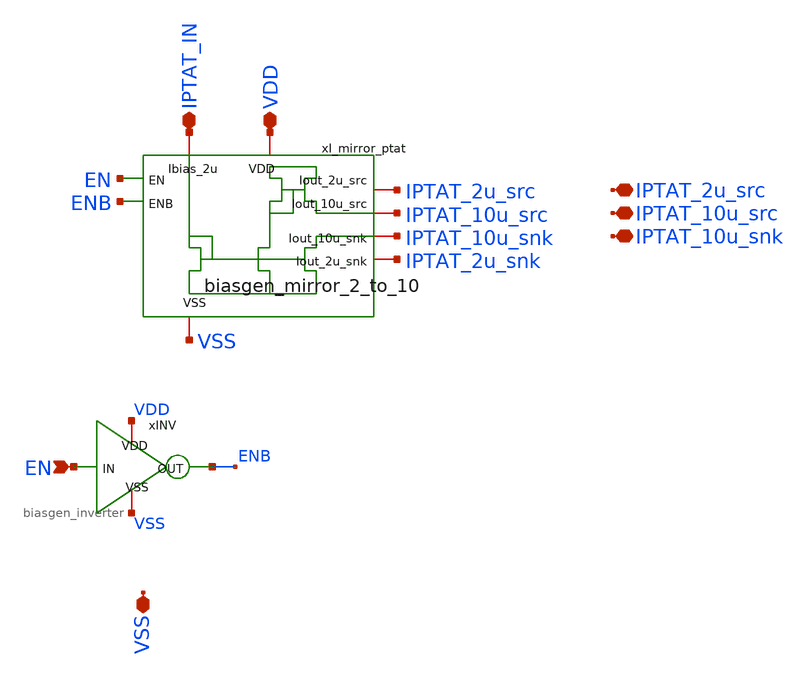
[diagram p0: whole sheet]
** sch_path: designs/libs/core_biasgen/biasgen_v2/biasgen_v2.sch
**.subckt biasgen_v2 VSS IPTAT_IN IPTAT_2u_src IPTAT_10u_snk VDD EN IPTAT_10u_src
*.iopin VSS
*.iopin IPTAT_IN
*.iopin IPTAT_2u_src
*.iopin IPTAT_10u_snk
*.iopin VDD
*.ipin EN
*.iopin IPTAT_10u_src
xI_mirror_ptat VDD IPTAT_IN EN ENB IPTAT_10u_src IPTAT_10u_snk VSS IPTAT_2u_src IPTAT_2u_snk
+ biasgen_mirror_2_to_10
xINV VDD EN ENB VSS biasgen_inverter
**.ends

* expanding   symbol:  libs/core_biasgen/biasgen_mirror_2_to_10/biasgen_mirror_2_to_10.sym # of
*+ pins=9
** sym_path: designs/libs/core_biasgen/biasgen_mirror_2_to_10/biasgen_mirror_2_to_10.sym
** sch_path: designs/libs/core_biasgen/biasgen_mirror_2_to_10/biasgen_mirror_2_to_10.sch
.subckt biasgen_mirror_2_to_10 VDD Ibias_2u EN ENB Iout_10u_src Iout_10u_snk VSS Iout_2u_src
+ Iout_2u_snk
*.iopin Ibias_2u
*.iopin VDD
*.iopin VSS
*.iopin Iout_10u_snk
*.iopin Iout_10u_src
*.ipin EN
*.ipin ENB
*.iopin Iout_2u_src
*.iopin Iout_2u_snk
XMnref0 net1 vnref VSS VSS nfet_05v0 L=2u W=0.5u nf=1 ad='int((nf+1)/2) * W/nf * 0.18u' as='int((nf+2)/2) * W/nf * 0.18u'
+ pd='2*int((nf+1)/2) * (W/nf + 0.18u)' ps='2*int((nf+2)/2) * (W/nf + 0.18u)' nrd='0.18u / W' nrs='0.18u / W'
+ sa=0 sb=0 sd=0 m=2
XMncas0 vnref vncas net1 VSS nfet_05v0 L=0.8u W=0.5u nf=1 ad='int((nf+1)/2) * W/nf * 0.18u' as='int((nf+2)/2) * W/nf * 0.18u'
+ pd='2*int((nf+1)/2) * (W/nf + 0.18u)' ps='2*int((nf+2)/2) * (W/nf + 0.18u)' nrd='0.18u / W' nrs='0.18u / W'
+ sa=0 sb=0 sd=0 m=2
XMnenbias Ibias_2u EN vncas vncas nfet_05v0 L=0.6u W=2u nf=1 ad='int((nf+1)/2) * W/nf * 0.18u' as='int((nf+2)/2) * W/nf * 0.18u'
+ pd='2*int((nf+1)/2) * (W/nf + 0.18u)' ps='2*int((nf+2)/2) * (W/nf + 0.18u)' nrd='0.18u / W' nrs='0.18u / W'
+ sa=0 sb=0 sd=0 m=1
XMnref1 net2 vnref VSS VSS nfet_05v0 L=2u W=0.5u nf=1 ad='int((nf+1)/2) * W/nf * 0.18u' as='int((nf+2)/2) * W/nf * 0.18u'
+ pd='2*int((nf+1)/2) * (W/nf + 0.18u)' ps='2*int((nf+2)/2) * (W/nf + 0.18u)' nrd='0.18u / W' nrs='0.18u / W'
+ sa=0 sb=0 sd=0 m=2
XMncas1 vpcas vncas net2 VSS nfet_05v0 L=0.8u W=0.5u nf=1 ad='int((nf+1)/2) * W/nf * 0.18u' as='int((nf+2)/2) * W/nf * 0.18u'
+ pd='2*int((nf+1)/2) * (W/nf + 0.18u)' ps='2*int((nf+2)/2) * (W/nf + 0.18u)' nrd='0.18u / W' nrs='0.18u / W'
+ sa=0 sb=0 sd=0 m=2
XMpref1 net3 vpref VDD VDD pfet_05v0 L=1.5u W=1u nf=1 ad='int((nf+1)/2) * W/nf * 0.18u' as='int((nf+2)/2) * W/nf * 0.18u'
+ pd='2*int((nf+1)/2) * (W/nf + 0.18u)' ps='2*int((nf+2)/2) * (W/nf + 0.18u)' nrd='0.18u / W' nrs='0.18u / W'
+ sa=0 sb=0 sd=0 m=2
XMpcas0 vpref vpcas net3 VDD pfet_05v0 L=0.8u W=1u nf=1 ad='int((nf+1)/2) * W/nf * 0.18u' as='int((nf+2)/2) * W/nf * 0.18u'
+ pd='2*int((nf+1)/2) * (W/nf + 0.18u)' ps='2*int((nf+2)/2) * (W/nf + 0.18u)' nrd='0.18u / W' nrs='0.18u / W'
+ sa=0 sb=0 sd=0 m=2
XMpcas1 vpcas vpcas VDD VDD pfet_05v0 L=6u W=1u nf=1 ad='int((nf+1)/2) * W/nf * 0.18u' as='int((nf+2)/2) * W/nf * 0.18u'
+ pd='2*int((nf+1)/2) * (W/nf + 0.18u)' ps='2*int((nf+2)/2) * (W/nf + 0.18u)' nrd='0.18u / W' nrs='0.18u / W'
+ sa=0 sb=0 sd=0 m=2
XMnref2 net4 vnref VSS VSS nfet_05v0 L=2u W=0.5u nf=1 ad='int((nf+1)/2) * W/nf * 0.18u' as='int((nf+2)/2) * W/nf * 0.18u'
+ pd='2*int((nf+1)/2) * (W/nf + 0.18u)' ps='2*int((nf+2)/2) * (W/nf + 0.18u)' nrd='0.18u / W' nrs='0.18u / W'
+ sa=0 sb=0 sd=0 m=2
XMncas2 vpref vncas net4 VSS nfet_05v0 L=0.8u W=0.5u nf=1 ad='int((nf+1)/2) * W/nf * 0.18u' as='int((nf+2)/2) * W/nf * 0.18u'
+ pd='2*int((nf+1)/2) * (W/nf + 0.18u)' ps='2*int((nf+2)/2) * (W/nf + 0.18u)' nrd='0.18u / W' nrs='0.18u / W'
+ sa=0 sb=0 sd=0 m=2
XMpref2 net5 vpref VDD VDD pfet_05v0 L=1.5u W=1u nf=1 ad='int((nf+1)/2) * W/nf * 0.18u' as='int((nf+2)/2) * W/nf * 0.18u'
+ pd='2*int((nf+1)/2) * (W/nf + 0.18u)' ps='2*int((nf+2)/2) * (W/nf + 0.18u)' nrd='0.18u / W' nrs='0.18u / W'
+ sa=0 sb=0 sd=0 m=10
XMpcas2 Iout_10u_src vpcas net5 VDD pfet_05v0 L=0.8u W=1u nf=1 ad='int((nf+1)/2) * W/nf * 0.18u' as='int((nf+2)/2) * W/nf * 0.18u'
+ pd='2*int((nf+1)/2) * (W/nf + 0.18u)' ps='2*int((nf+2)/2) * (W/nf + 0.18u)' nrd='0.18u / W' nrs='0.18u / W'
+ sa=0 sb=0 sd=0 m=10
XMnref3 net6 vnref VSS VSS nfet_05v0 L=2u W=0.5u nf=1 ad='int((nf+1)/2) * W/nf * 0.18u' as='int((nf+2)/2) * W/nf * 0.18u'
+ pd='2*int((nf+1)/2) * (W/nf + 0.18u)' ps='2*int((nf+2)/2) * (W/nf + 0.18u)' nrd='0.18u / W' nrs='0.18u / W'
+ sa=0 sb=0 sd=0 m=10
XMncas3 Iout_10u_snk vncas net6 VSS nfet_05v0 L=0.8u W=0.5u nf=1 ad='int((nf+1)/2) * W/nf * 0.18u' as='int((nf+2)/2) * W/nf * 0.18u'
+ pd='2*int((nf+1)/2) * (W/nf + 0.18u)' ps='2*int((nf+2)/2) * (W/nf + 0.18u)' nrd='0.18u / W' nrs='0.18u / W'
+ sa=0 sb=0 sd=0 m=10
XMnennref vnref ENB VSS VSS nfet_05v0 L=0.6u W=2u nf=1 ad='int((nf+1)/2) * W/nf * 0.18u' as='int((nf+2)/2) * W/nf * 0.18u'
+ pd='2*int((nf+1)/2) * (W/nf + 0.18u)' ps='2*int((nf+2)/2) * (W/nf + 0.18u)' nrd='0.18u / W' nrs='0.18u / W'
+ sa=0 sb=0 sd=0 m=1
XMnenncas vncas ENB VSS VSS nfet_05v0 L=0.6u W=2u nf=1 ad='int((nf+1)/2) * W/nf * 0.18u' as='int((nf+2)/2) * W/nf * 0.18u'
+ pd='2*int((nf+1)/2) * (W/nf + 0.18u)' ps='2*int((nf+2)/2) * (W/nf + 0.18u)' nrd='0.18u / W' nrs='0.18u / W'
+ sa=0 sb=0 sd=0 m=1
XMpcas3 vpref EN VDD VDD pfet_05v0 L=0.5u W=1u nf=1 ad='int((nf+1)/2) * W/nf * 0.18u' as='int((nf+2)/2) * W/nf * 0.18u'
+ pd='2*int((nf+1)/2) * (W/nf + 0.18u)' ps='2*int((nf+2)/2) * (W/nf + 0.18u)' nrd='0.18u / W' nrs='0.18u / W'
+ sa=0 sb=0 sd=0 m=1
XMpcas4 vpcas EN VDD VDD pfet_05v0 L=0.5u W=1u nf=1 ad='int((nf+1)/2) * W/nf * 0.18u' as='int((nf+2)/2) * W/nf * 0.18u'
+ pd='2*int((nf+1)/2) * (W/nf + 0.18u)' ps='2*int((nf+2)/2) * (W/nf + 0.18u)' nrd='0.18u / W' nrs='0.18u / W'
+ sa=0 sb=0 sd=0 m=1
XMpref3 net7 vpref VDD VDD pfet_05v0 L=1.5u W=1u nf=1 ad='int((nf+1)/2) * W/nf * 0.18u' as='int((nf+2)/2) * W/nf * 0.18u'
+ pd='2*int((nf+1)/2) * (W/nf + 0.18u)' ps='2*int((nf+2)/2) * (W/nf + 0.18u)' nrd='0.18u / W' nrs='0.18u / W'
+ sa=0 sb=0 sd=0 m=2
XMpcas5 Iout_2u_src vpcas net7 VDD pfet_05v0 L=0.8u W=1u nf=1 ad='int((nf+1)/2) * W/nf * 0.18u' as='int((nf+2)/2) * W/nf * 0.18u'
+ pd='2*int((nf+1)/2) * (W/nf + 0.18u)' ps='2*int((nf+2)/2) * (W/nf + 0.18u)' nrd='0.18u / W' nrs='0.18u / W'
+ sa=0 sb=0 sd=0 m=2
XMnref4 net8 vnref VSS VSS nfet_05v0 L=2u W=0.5u nf=1 ad='int((nf+1)/2) * W/nf * 0.18u' as='int((nf+2)/2) * W/nf * 0.18u'
+ pd='2*int((nf+1)/2) * (W/nf + 0.18u)' ps='2*int((nf+2)/2) * (W/nf + 0.18u)' nrd='0.18u / W' nrs='0.18u / W'
+ sa=0 sb=0 sd=0 m=2
XMncas4 Iout_2u_snk vncas net8 VSS nfet_05v0 L=0.8u W=0.5u nf=1 ad='int((nf+1)/2) * W/nf * 0.18u' as='int((nf+2)/2) * W/nf * 0.18u'
+ pd='2*int((nf+1)/2) * (W/nf + 0.18u)' ps='2*int((nf+2)/2) * (W/nf + 0.18u)' nrd='0.18u / W' nrs='0.18u / W'
+ sa=0 sb=0 sd=0 m=2
XMnref_dumm_L VSS VSS VSS VSS nfet_05v0 L=2u W=0.5u nf=1 ad='int((nf+1)/2) * W/nf * 0.18u' as='int((nf+2)/2) * W/nf * 0.18u'
+ pd='2*int((nf+1)/2) * (W/nf + 0.18u)' ps='2*int((nf+2)/2) * (W/nf + 0.18u)' nrd='0.18u / W' nrs='0.18u / W'
+ sa=0 sb=0 sd=0 m=2
XMncas_dumm_L VSS VSS VSS VSS nfet_05v0 L=0.8u W=0.5u nf=1 ad='int((nf+1)/2) * W/nf * 0.18u' as='int((nf+2)/2) * W/nf * 0.18u'
+ pd='2*int((nf+1)/2) * (W/nf + 0.18u)' ps='2*int((nf+2)/2) * (W/nf + 0.18u)' nrd='0.18u / W' nrs='0.18u / W'
+ sa=0 sb=0 sd=0 m=2
XMpref_dumm_L[1] VDD VDD VDD VDD pfet_05v0 L=1.5u W=1u nf=1 ad='int((nf+1)/2) * W/nf * 0.18u' as='int((nf+2)/2) * W/nf * 0.18u'
+ pd='2*int((nf+1)/2) * (W/nf + 0.18u)' ps='2*int((nf+2)/2) * (W/nf + 0.18u)' nrd='0.18u / W' nrs='0.18u / W'
+ sa=0 sb=0 sd=0 m=1
XMpref_dumm_L[0] VDD VDD VDD VDD pfet_05v0 L=1.5u W=1u nf=1 ad='int((nf+1)/2) * W/nf * 0.18u' as='int((nf+2)/2) * W/nf * 0.18u'
+ pd='2*int((nf+1)/2) * (W/nf + 0.18u)' ps='2*int((nf+2)/2) * (W/nf + 0.18u)' nrd='0.18u / W' nrs='0.18u / W'
+ sa=0 sb=0 sd=0 m=1
XMpcas_dumm_L[1] VDD VDD VDD VDD pfet_05v0 L=0.8u W=1u nf=1 ad='int((nf+1)/2) * W/nf * 0.18u' as='int((nf+2)/2) * W/nf * 0.18u'
+ pd='2*int((nf+1)/2) * (W/nf + 0.18u)' ps='2*int((nf+2)/2) * (W/nf + 0.18u)' nrd='0.18u / W' nrs='0.18u / W'
+ sa=0 sb=0 sd=0 m=1
XMpcas_dumm_L[0] VDD VDD VDD VDD pfet_05v0 L=0.8u W=1u nf=1 ad='int((nf+1)/2) * W/nf * 0.18u' as='int((nf+2)/2) * W/nf * 0.18u'
+ pd='2*int((nf+1)/2) * (W/nf + 0.18u)' ps='2*int((nf+2)/2) * (W/nf + 0.18u)' nrd='0.18u / W' nrs='0.18u / W'
+ sa=0 sb=0 sd=0 m=1
XMpcasref_dumm_L[3] VDD VDD VDD VDD pfet_05v0 L=6u W=1u nf=1 ad='int((nf+1)/2) * W/nf * 0.18u' as='int((nf+2)/2) * W/nf * 0.18u'
+ pd='2*int((nf+1)/2) * (W/nf + 0.18u)' ps='2*int((nf+2)/2) * (W/nf + 0.18u)' nrd='0.18u / W' nrs='0.18u / W'
+ sa=0 sb=0 sd=0 m=1
XMpcasref_dumm_L[2] VDD VDD VDD VDD pfet_05v0 L=6u W=1u nf=1 ad='int((nf+1)/2) * W/nf * 0.18u' as='int((nf+2)/2) * W/nf * 0.18u'
+ pd='2*int((nf+1)/2) * (W/nf + 0.18u)' ps='2*int((nf+2)/2) * (W/nf + 0.18u)' nrd='0.18u / W' nrs='0.18u / W'
+ sa=0 sb=0 sd=0 m=1
XMpcasref_dumm_L[1] VDD VDD VDD VDD pfet_05v0 L=6u W=1u nf=1 ad='int((nf+1)/2) * W/nf * 0.18u' as='int((nf+2)/2) * W/nf * 0.18u'
+ pd='2*int((nf+1)/2) * (W/nf + 0.18u)' ps='2*int((nf+2)/2) * (W/nf + 0.18u)' nrd='0.18u / W' nrs='0.18u / W'
+ sa=0 sb=0 sd=0 m=1
XMpcasref_dumm_L[0] VDD VDD VDD VDD pfet_05v0 L=6u W=1u nf=1 ad='int((nf+1)/2) * W/nf * 0.18u' as='int((nf+2)/2) * W/nf * 0.18u'
+ pd='2*int((nf+1)/2) * (W/nf + 0.18u)' ps='2*int((nf+2)/2) * (W/nf + 0.18u)' nrd='0.18u / W' nrs='0.18u / W'
+ sa=0 sb=0 sd=0 m=1
XRPcas[7] vr_ncas[7] vncas VSS ppolyf_u_1k_6p0 r_width=1e-6 r_length=4.5e-6 m=1
XRPcas[6] vr_ncas[6] vr_ncas[7] VSS ppolyf_u_1k_6p0 r_width=1e-6 r_length=4.5e-6 m=1
XRPcas[5] vr_ncas[5] vr_ncas[6] VSS ppolyf_u_1k_6p0 r_width=1e-6 r_length=4.5e-6 m=1
XRPcas[4] vr_ncas[4] vr_ncas[5] VSS ppolyf_u_1k_6p0 r_width=1e-6 r_length=4.5e-6 m=1
XRPcas[3] vr_ncas[3] vr_ncas[4] VSS ppolyf_u_1k_6p0 r_width=1e-6 r_length=4.5e-6 m=1
XRPcas[2] vr_ncas[2] vr_ncas[3] VSS ppolyf_u_1k_6p0 r_width=1e-6 r_length=4.5e-6 m=1
XRPcas[1] vr_ncas[1] vr_ncas[2] VSS ppolyf_u_1k_6p0 r_width=1e-6 r_length=4.5e-6 m=1
XRPcas[0] vnref vr_ncas[1] VSS ppolyf_u_1k_6p0 r_width=1e-6 r_length=4.5e-6 m=1
.ends


* expanding   symbol:  libs/core_biasgen/biasgen_inverter/biasgen_inverter.sym # of pins=4
** sym_path: designs/libs/core_biasgen/biasgen_inverter/biasgen_inverter.sym
** sch_path: designs/libs/core_biasgen/biasgen_inverter/biasgen_inverter.sch
.subckt biasgen_inverter VDD IN OUT VSS
*.iopin VDD
*.iopin VSS
*.ipin IN
*.opin OUT
XMINV1 OUT IN VSS VSS nfet_05v0 L=0.60u W=0.50u nf=1 ad='int((nf+1)/2) * W/nf * 0.18u' as='int((nf+2)/2) * W/nf * 0.18u'
+ pd='2*int((nf+1)/2) * (W/nf + 0.18u)' ps='2*int((nf+2)/2) * (W/nf + 0.18u)' nrd='0.18u / W' nrs='0.18u / W'
+ sa=0 sb=0 sd=0 m=1
XMINV2 OUT IN VDD VDD pfet_05v0 L=0.50u W=0.60u nf=1 ad='int((nf+1)/2) * W/nf * 0.18u' as='int((nf+2)/2) * W/nf * 0.18u'
+ pd='2*int((nf+1)/2) * (W/nf + 0.18u)' ps='2*int((nf+2)/2) * (W/nf + 0.18u)' nrd='0.18u / W' nrs='0.18u / W'
+ sa=0 sb=0 sd=0 m=1
.ends

.end
